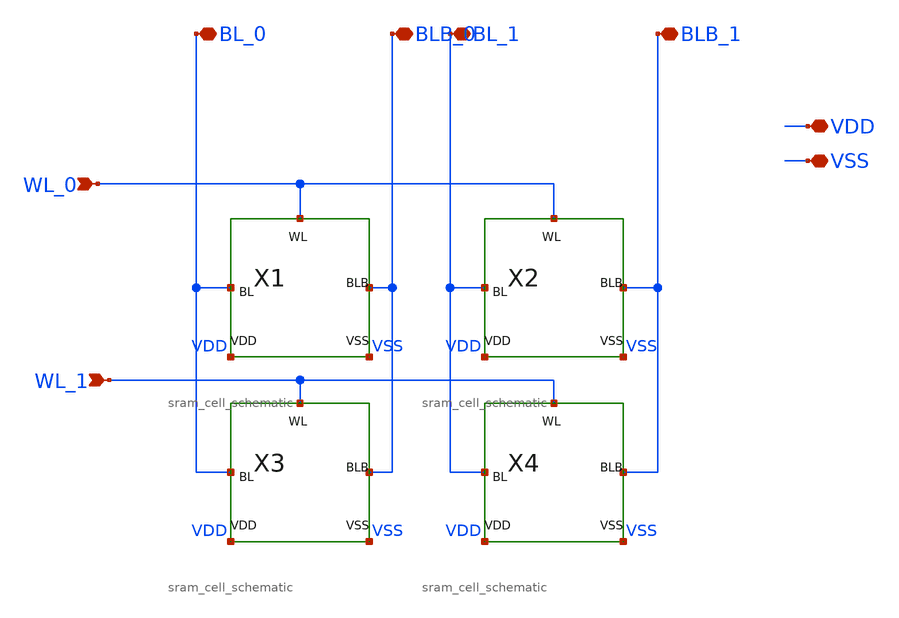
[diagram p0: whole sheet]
** sch_path: SRAM/2x2/schematic/sram_2x2_schematic.sch
**.subckt sram_2x2_schematic WL_0 WL_1 BL_0 BLB_0 BL_1 BLB_1 VDD VSS
*.ipin WL_0
*.ipin WL_1
*.iopin BL_0
*.iopin BLB_0
*.iopin BL_1
*.iopin BLB_1
*.iopin VDD
*.iopin VSS
X1 WL_0 BL_0 BLB_0 VDD VSS sram_cell_schematic
X2 WL_0 BL_1 BLB_1 VDD VSS sram_cell_schematic
X3 WL_1 BL_0 BLB_0 VDD VSS sram_cell_schematic
X4 WL_1 BL_1 BLB_1 VDD VSS sram_cell_schematic
**.ends

* expanding   symbol:  sram_cell_schematic.sym # of pins=5
** sym_path: SRAM/cell/schematic/sram_cell_schematic.sym
** sch_path: SRAM/cell/schematic/sram_cell_schematic.sch
.subckt sram_cell_schematic WL BL BLB VDD VSS
*.ipin WL
*.iopin BL
*.iopin BLB
*.iopin VDD
*.iopin VSS
M4 VSS Q QB VSS nfet w=3.6u l=0.6u m=1
M5 QB Q VDD VDD pfet w=3.6u l=0.6u m=1
M6 Q QB VDD VDD pfet w=3.6u l=0.6u m=1
M1 Q WL BL VSS nfet w=1.8u l=0.6u m=1
M3 VSS QB Q VSS nfet w=3.6u l=0.6u m=1
M2 BLB WL QB VSS nfet w=1.8u l=0.6u m=1
.ends

.end
